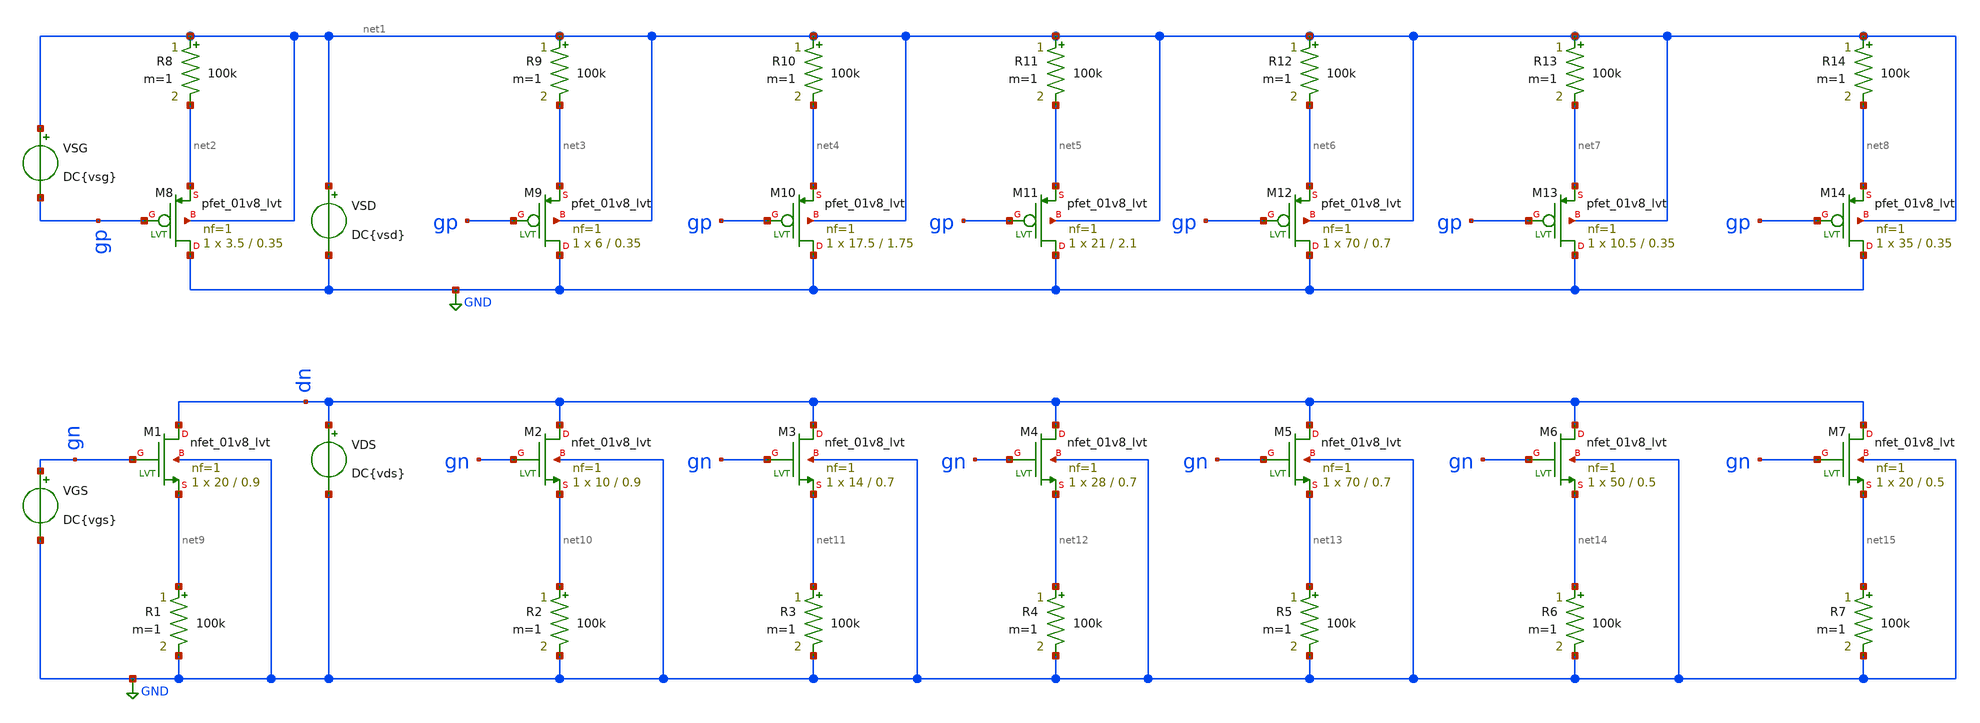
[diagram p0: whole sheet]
** sch_path: XSCHEM/VTH_characterization_lvt_01v8_Body_Effect.sch
**.subckt VTH_characterization_lvt_01v8_Body_Effect
XM1 dn gn net9 GND sky130_fd_pr__nfet_01v8_lvt L=0.9 W=20 nf=1 ad='int((nf+1)/2) * W/nf * 0.29' as='int((nf+2)/2) * W/nf * 0.29'
+ pd='2*int((nf+1)/2) * (W/nf + 0.29)' ps='2*int((nf+2)/2) * (W/nf + 0.29)' nrd='0.29 / W' nrs='0.29 / W'
+ sa=0 sb=0 sd=0 mult=1 m=1
XM2 dn gn net10 GND sky130_fd_pr__nfet_01v8_lvt L=0.9 W=10 nf=1 ad='int((nf+1)/2) * W/nf * 0.29' as='int((nf+2)/2) * W/nf * 0.29'
+ pd='2*int((nf+1)/2) * (W/nf + 0.29)' ps='2*int((nf+2)/2) * (W/nf + 0.29)' nrd='0.29 / W' nrs='0.29 / W'
+ sa=0 sb=0 sd=0 mult=1 m=1
VGS gn GND DC{vgs}
VDS dn GND DC{vds}
XM3 dn gn net11 GND sky130_fd_pr__nfet_01v8_lvt L=0.7 W=14 nf=1 ad='int((nf+1)/2) * W/nf * 0.29' as='int((nf+2)/2) * W/nf * 0.29'
+ pd='2*int((nf+1)/2) * (W/nf + 0.29)' ps='2*int((nf+2)/2) * (W/nf + 0.29)' nrd='0.29 / W' nrs='0.29 / W'
+ sa=0 sb=0 sd=0 mult=1 m=1
XM4 dn gn net12 GND sky130_fd_pr__nfet_01v8_lvt L=0.7 W=28 nf=1 ad='int((nf+1)/2) * W/nf * 0.29' as='int((nf+2)/2) * W/nf * 0.29'
+ pd='2*int((nf+1)/2) * (W/nf + 0.29)' ps='2*int((nf+2)/2) * (W/nf + 0.29)' nrd='0.29 / W' nrs='0.29 / W'
+ sa=0 sb=0 sd=0 mult=1 m=1
XM5 dn gn net13 GND sky130_fd_pr__nfet_01v8_lvt L=0.7 W=70 nf=1 ad='int((nf+1)/2) * W/nf * 0.29' as='int((nf+2)/2) * W/nf * 0.29'
+ pd='2*int((nf+1)/2) * (W/nf + 0.29)' ps='2*int((nf+2)/2) * (W/nf + 0.29)' nrd='0.29 / W' nrs='0.29 / W'
+ sa=0 sb=0 sd=0 mult=1 m=1
XM6 dn gn net14 GND sky130_fd_pr__nfet_01v8_lvt L=0.5 W=50 nf=1 ad='int((nf+1)/2) * W/nf * 0.29' as='int((nf+2)/2) * W/nf * 0.29'
+ pd='2*int((nf+1)/2) * (W/nf + 0.29)' ps='2*int((nf+2)/2) * (W/nf + 0.29)' nrd='0.29 / W' nrs='0.29 / W'
+ sa=0 sb=0 sd=0 mult=1 m=1
VSG net1 gp DC{vsg}
VSD net1 GND DC{vsd}
XM7 dn gn net15 GND sky130_fd_pr__nfet_01v8_lvt L=0.5 W=20 nf=1 ad='int((nf+1)/2) * W/nf * 0.29' as='int((nf+2)/2) * W/nf * 0.29'
+ pd='2*int((nf+1)/2) * (W/nf + 0.29)' ps='2*int((nf+2)/2) * (W/nf + 0.29)' nrd='0.29 / W' nrs='0.29 / W'
+ sa=0 sb=0 sd=0 mult=1 m=1
XM8 GND gp net2 net1 sky130_fd_pr__pfet_01v8_lvt L=0.35 W=3.5 nf=1 ad='int((nf+1)/2) * W/nf * 0.29' as='int((nf+2)/2) * W/nf * 0.29'
+ pd='2*int((nf+1)/2) * (W/nf + 0.29)' ps='2*int((nf+2)/2) * (W/nf + 0.29)' nrd='0.29 / W' nrs='0.29 / W'
+ sa=0 sb=0 sd=0 mult=1 m=1
XM9 GND gp net3 net1 sky130_fd_pr__pfet_01v8_lvt L=0.35 W=6 nf=1 ad='int((nf+1)/2) * W/nf * 0.29' as='int((nf+2)/2) * W/nf * 0.29'
+ pd='2*int((nf+1)/2) * (W/nf + 0.29)' ps='2*int((nf+2)/2) * (W/nf + 0.29)' nrd='0.29 / W' nrs='0.29 / W'
+ sa=0 sb=0 sd=0 mult=1 m=1
XM10 GND gp net4 net1 sky130_fd_pr__pfet_01v8_lvt L=1.75 W=17.5 nf=1 ad='int((nf+1)/2) * W/nf * 0.29'
+ as='int((nf+2)/2) * W/nf * 0.29' pd='2*int((nf+1)/2) * (W/nf + 0.29)' ps='2*int((nf+2)/2) * (W/nf + 0.29)'
+ nrd='0.29 / W' nrs='0.29 / W' sa=0 sb=0 sd=0 mult=1 m=1
XM11 GND gp net5 net1 sky130_fd_pr__pfet_01v8_lvt L=2.1 W=21 nf=1 ad='int((nf+1)/2) * W/nf * 0.29' as='int((nf+2)/2) * W/nf * 0.29'
+ pd='2*int((nf+1)/2) * (W/nf + 0.29)' ps='2*int((nf+2)/2) * (W/nf + 0.29)' nrd='0.29 / W' nrs='0.29 / W'
+ sa=0 sb=0 sd=0 mult=1 m=1
XM12 GND gp net6 net1 sky130_fd_pr__pfet_01v8_lvt L=0.7 W=70 nf=1 ad='int((nf+1)/2) * W/nf * 0.29' as='int((nf+2)/2) * W/nf * 0.29'
+ pd='2*int((nf+1)/2) * (W/nf + 0.29)' ps='2*int((nf+2)/2) * (W/nf + 0.29)' nrd='0.29 / W' nrs='0.29 / W'
+ sa=0 sb=0 sd=0 mult=1 m=1
XM13 GND gp net7 net1 sky130_fd_pr__pfet_01v8_lvt L=0.35 W=10.5 nf=1 ad='int((nf+1)/2) * W/nf * 0.29'
+ as='int((nf+2)/2) * W/nf * 0.29' pd='2*int((nf+1)/2) * (W/nf + 0.29)' ps='2*int((nf+2)/2) * (W/nf + 0.29)'
+ nrd='0.29 / W' nrs='0.29 / W' sa=0 sb=0 sd=0 mult=1 m=1
XM14 GND gp net8 net1 sky130_fd_pr__pfet_01v8_lvt L=0.35 W=35 nf=1 ad='int((nf+1)/2) * W/nf * 0.29' as='int((nf+2)/2) * W/nf * 0.29'
+ pd='2*int((nf+1)/2) * (W/nf + 0.29)' ps='2*int((nf+2)/2) * (W/nf + 0.29)' nrd='0.29 / W' nrs='0.29 / W'
+ sa=0 sb=0 sd=0 mult=1 m=1
R1 net9 GND 100k m=1
R2 net10 GND 100k m=1
R3 net11 GND 100k m=1
R4 net12 GND 100k m=1
R5 net13 GND 100k m=1
R6 net14 GND 100k m=1
R7 net15 GND 100k m=1
R8 net1 net2 100k m=1
R9 net1 net3 100k m=1
R10 net1 net4 100k m=1
R11 net1 net5 100k m=1
R12 net1 net6 100k m=1
R13 net1 net7 100k m=1
R14 net1 net8 100k m=1
**** begin user architecture code



* Parameters
.param vds = 1.8
.param vgs = 0.9
.param vsd = 1.8
.param vsg = 0.9
.options TEMPS = 27.0

* Models
.lib /home/karlajcm/skywater130/skywater-pdk/libraries/sky130_fd_pr/latest/models/sky130.lib.spice TT

* Data to save
.save all  @M.XM1.msky130_fd_pr__nfet_01v8_lvt[id]  @M.XM1.msky130_fd_pr__nfet_01v8_lvt[gm]  @M.XM1.msky130_fd_pr__nfet_01v8_lvt[vth]  @M.XM1.msky130_fd_pr__nfet_01v8_lvt[vds]  @M.XM1.msky130_fd_pr__nfet_01v8_lvt[vdsat]  @M.XM1.msky130_fd_pr__nfet_01v8_lvt[vgs]  @M.XM1.msky130_fd_pr__nfet_01v8_lvt[cgg]  @M.XM2.msky130_fd_pr__nfet_01v8_lvt[id]  @M.XM2.msky130_fd_pr__nfet_01v8_lvt[gm]  @M.XM2.msky130_fd_pr__nfet_01v8_lvt[vth]  @M.XM2.msky130_fd_pr__nfet_01v8_lvt[vds]  @M.XM2.msky130_fd_pr__nfet_01v8_lvt[vdsat]  @M.XM2.msky130_fd_pr__nfet_01v8_lvt[vgs]  @M.XM2.msky130_fd_pr__nfet_01v8_lvt[cgg]  @M.XM3.msky130_fd_pr__nfet_01v8_lvt[id]  @M.XM3.msky130_fd_pr__nfet_01v8_lvt[gm]  @M.XM3.msky130_fd_pr__nfet_01v8_lvt[vth]  @M.XM3.msky130_fd_pr__nfet_01v8_lvt[vds]  @M.XM3.msky130_fd_pr__nfet_01v8_lvt[vdsat]  @M.XM3.msky130_fd_pr__nfet_01v8_lvt[vgs]  @M.XM3.msky130_fd_pr__nfet_01v8_lvt[cgg]  @M.XM4.msky130_fd_pr__nfet_01v8_lvt[id]  @M.XM4.msky130_fd_pr__nfet_01v8_lvt[gm]  @M.XM4.msky130_fd_pr__nfet_01v8_lvt[vth]  @M.XM4.msky130_fd_pr__nfet_01v8_lvt[vds]  @M.XM4.msky130_fd_pr__nfet_01v8_lvt[vdsat]  @M.XM4.msky130_fd_pr__nfet_01v8_lvt[vgs]  @M.XM4.msky130_fd_pr__nfet_01v8_lvt[cgg]  @M.XM5.msky130_fd_pr__nfet_01v8_lvt[id]  @M.XM5.msky130_fd_pr__nfet_01v8_lvt[gm]  @M.XM5.msky130_fd_pr__nfet_01v8_lvt[vth]  @M.XM5.msky130_fd_pr__nfet_01v8_lvt[vds]  @M.XM5.msky130_fd_pr__nfet_01v8_lvt[vdsat]  @M.XM5.msky130_fd_pr__nfet_01v8_lvt[vgs]  @M.XM5.msky130_fd_pr__nfet_01v8_lvt[cgg]  @M.XM6.msky130_fd_pr__nfet_01v8_lvt[id]  @M.XM6.msky130_fd_pr__nfet_01v8_lvt[gm]  @M.XM6.msky130_fd_pr__nfet_01v8_lvt[vth]  @M.XM6.msky130_fd_pr__nfet_01v8_lvt[vds]  @M.XM6.msky130_fd_pr__nfet_01v8_lvt[vdsat]  @M.XM6.msky130_fd_pr__nfet_01v8_lvt[vgs]  @M.XM6.msky130_fd_pr__nfet_01v8_lvt[cgg]  @M.XM7.msky130_fd_pr__nfet_01v8_lvt[id]  @M.XM7.msky130_fd_pr__nfet_01v8_lvt[gm]  @M.XM7.msky130_fd_pr__nfet_01v8_lvt[vth]  @M.XM7.msky130_fd_pr__nfet_01v8_lvt[vds]  @M.XM7.msky130_fd_pr__nfet_01v8_lvt[vdsat]  @M.XM7.msky130_fd_pr__nfet_01v8_lvt[vgs]  @M.XM7.msky130_fd_pr__nfet_01v8_lvt[cgg]  @M.XM8.msky130_fd_pr__pfet_01v8_lvt[id]  @M.XM8.msky130_fd_pr__pfet_01v8_lvt[gm]  @M.XM8.msky130_fd_pr__pfet_01v8_lvt[vth]  @M.XM8.msky130_fd_pr__pfet_01v8_lvt[vds]  @M.XM8.msky130_fd_pr__pfet_01v8_lvt[vdsat]  @M.XM8.msky130_fd_pr__pfet_01v8_lvt[vgs]  @M.XM8.msky130_fd_pr__pfet_01v8_lvt[cgg]  @M.XM9.msky130_fd_pr__pfet_01v8_lvt[id]  @M.XM9.msky130_fd_pr__pfet_01v8_lvt[gm]  @M.XM9.msky130_fd_pr__pfet_01v8_lvt[vth]  @M.XM9.msky130_fd_pr__pfet_01v8_lvt[vds]  @M.XM9.msky130_fd_pr__pfet_01v8_lvt[vdsat]  @M.XM9.msky130_fd_pr__pfet_01v8_lvt[vgs]  @M.XM9.msky130_fd_pr__pfet_01v8_lvt[cgg]  @M.XM10.msky130_fd_pr__pfet_01v8_lvt[id]  @M.XM10.msky130_fd_pr__pfet_01v8_lvt[gm]  @M.XM10.msky130_fd_pr__pfet_01v8_lvt[vth]  @M.XM10.msky130_fd_pr__pfet_01v8_lvt[vds]  @M.XM10.msky130_fd_pr__pfet_01v8_lvt[vdsat]  @M.XM10.msky130_fd_pr__pfet_01v8_lvt[vgs]  @M.XM10.msky130_fd_pr__pfet_01v8_lvt[cgg]  @M.XM11.msky130_fd_pr__pfet_01v8_lvt[id]  @M.XM11.msky130_fd_pr__pfet_01v8_lvt[gm]  @M.XM11.msky130_fd_pr__pfet_01v8_lvt[vth]  @M.XM11.msky130_fd_pr__pfet_01v8_lvt[vds]  @M.XM11.msky130_fd_pr__pfet_01v8_lvt[vdsat]  @M.XM11.msky130_fd_pr__pfet_01v8_lvt[vgs]  @M.XM11.msky130_fd_pr__pfet_01v8_lvt[cgg]  @M.XM12.msky130_fd_pr__pfet_01v8_lvt[id]  @M.XM12.msky130_fd_pr__pfet_01v8_lvt[gm]  @M.XM12.msky130_fd_pr__pfet_01v8_lvt[vth]  @M.XM12.msky130_fd_pr__pfet_01v8_lvt[vds]  @M.XM12.msky130_fd_pr__pfet_01v8_lvt[vdsat]  @M.XM12.msky130_fd_pr__pfet_01v8_lvt[vgs]  @M.XM12.msky130_fd_pr__pfet_01v8_lvt[cgg]  @M.XM13.msky130_fd_pr__pfet_01v8_lvt[id]  @M.XM13.msky130_fd_pr__pfet_01v8_lvt[gm]  @M.XM13.msky130_fd_pr__pfet_01v8_lvt[vth]  @M.XM13.msky130_fd_pr__pfet_01v8_lvt[vds]  @M.XM13.msky130_fd_pr__pfet_01v8_lvt[vdsat]  @M.XM13.msky130_fd_pr__pfet_01v8_lvt[vgs]  @M.XM13.msky130_fd_pr__pfet_01v8_lvt[cgg]  @M.XM14.msky130_fd_pr__pfet_01v8_lvt[id]  @M.XM14.msky130_fd_pr__pfet_01v8_lvt[gm]  @M.XM14.msky130_fd_pr__pfet_01v8_lvt[vth]  @M.XM14.msky130_fd_pr__pfet_01v8_lvt[vds]  @M.XM14.msky130_fd_pr__pfet_01v8_lvt[vdsat]  @M.XM14.msky130_fd_pr__pfet_01v8_lvt[vgs]  @M.XM14.msky130_fd_pr__pfet_01v8_lvt[cgg]

* Simulation
.control
  dc VDS 0 1.8 0.01 VGS 0 1.8 0.3 VSD 0 1.8 0.01 VSG 0 1.8 0.3
  setplot dc1
  plot @M.XM1.msky130_fd_pr__nfet_01v8_lvt[id] @M.XM2.msky130_fd_pr__nfet_01v8_lvt[id] @M.XM3.msky130_fd_pr__nfet_01v8_lvt[id]
+ @M.XM4.msky130_fd_pr__nfet_01v8_lvt[id] @M.XM5.msky130_fd_pr__nfet_01v8_lvt[id] @M.XM6.msky130_fd_pr__nfet_01v8_lvt[id]
+ @M.XM7.msky130_fd_pr__nfet_01v8_lvt[id] ylabel Id xlabel Vds title 'NMOS: Id vs Vds vs Vgs'
  plot @M.XM8.msky130_fd_pr__pfet_01v8_lvt[id] @M.XM9.msky130_fd_pr__pfet_01v8_lvt[id] @M.XM10.msky130_fd_pr__pfet_01v8_lvt[id]
+ @M.XM11.msky130_fd_pr__pfet_01v8_lvt[id] @M.XM12.msky130_fd_pr__pfet_01v8_lvt[id] @M.XM13.msky130_fd_pr__pfet_01v8_lvt[id]
+ @M.XM14.msky130_fd_pr__pfet_01v8_lvt[id] ylabel Id xlabel Vsd title 'PMOS:Id vs Vsd vs Vsg'
  set filetype = ascii
  write VTH_characterization_lvt_01v8_dc1.raw

  *alterparam vds = 0
  *alterparam vsd = 0
  *reset
  *dc VGS -1.8 1.8 0.01 VSG -1.8 1.8 0.01
  *setplot dc2
  *plot @M.XM1.msky130_fd_pr__nfet_01v8_lvt[cgg] @M.XM2.msky130_fd_pr__nfet_01v8_lvt[cgg] @M.XM3.msky130_fd_pr__nfet_01v8_lvt[cgg]
+ @M.XM4.msky130_fd_pr__nfet_01v8_lvt[cgg] @M.XM5.msky130_fd_pr__nfet_01v8_lvt[cgg] @M.XM6.msky130_fd_pr__nfet_01v8_lvt[cgg]
+ @M.XM7.msky130_fd_pr__nfet_01v8_lvt[cgg] ylabel Cgg xlabel Vgs title 'NMOS:Cgg vs Vgs'
  *plot @M.XM8.msky130_fd_pr__pfet_01v8_lvt[cgg] @M.XM9.msky130_fd_pr__pfet_01v8_lvt[cgg] @M.XM10.msky130_fd_pr__pfet_01v8_lvt[cgg]
+ @M.XM11.msky130_fd_pr__pfet_01v8_lvt[cgg] @M.XM12.msky130_fd_pr__pfet_01v8_lvt[cgg] @M.XM13.msky130_fd_pr__pfet_01v8_lvt[cgg]
+ @M.XM14.msky130_fd_pr__pfet_01v8_lvt[cgg] ylabel Cgg xlabel Vgs title 'PMOS:Cgg vs Vsg'
  *set filetype = ascii
  *write VTH_characterization_lvt_01v8_dc2.raw

  *reset
  *dc VGS -1.8 1.8 0.01 VSG -1.8 1.8 0.01
  *setplot dc3
  *plot @M.XM1.msky130_fd_pr__nfet_01v8_lvt[vth] @M.XM2.msky130_fd_pr__nfet_01v8_lvt[vth] @M.XM3.msky130_fd_pr__nfet_01v8_lvt[vth]
+ @M.XM4.msky130_fd_pr__nfet_01v8_lvt[vth] @M.XM5.msky130_fd_pr__nfet_01v8_lvt[vth] @M.XM6.msky130_fd_pr__nfet_01v8_lvt[vth]
+ @M.XM7.msky130_fd_pr__nfet_01v8_lvt[vth] ylabel Vth xlabel Vgs title 'NMOS:Vth vs Vgs'
  *plot @M.XM8.msky130_fd_pr__pfet_01v8_lvt[vth] @M.XM9.msky130_fd_pr__pfet_01v8_lvt[vth] @M.XM10.msky130_fd_pr__pfet_01v8_lvt[vth]
+ @M.XM11.msky130_fd_pr__pfet_01v8_lvt[vth] @M.XM12.msky130_fd_pr__pfet_01v8_lvt[vth] @M.XM13.msky130_fd_pr__pfet_01v8_lvt[vth]
+ @M.XM14.msky130_fd_pr__pfet_01v8_lvt[vth] ylabel Vth xlabel Vsg title 'PMOS:Vth vs Vsg'
  *set filetype = ascii
  *write VTH_characterization_lvt_01v8_dc3.raw

  reset
  unset filetype
  op
  save all
  write VTH_characterization_lvt_01v8.raw

.endc

.end


**** end user architecture code
**.ends
.GLOBAL GND
.end
